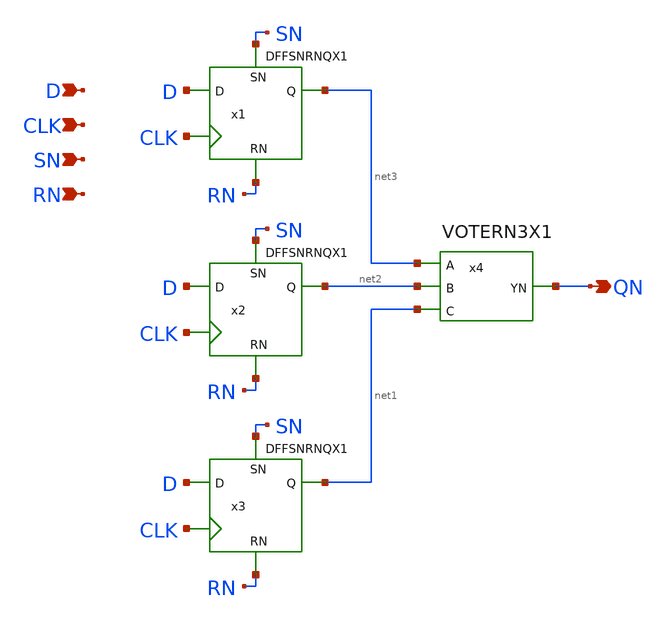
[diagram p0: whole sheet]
** sch_path: lib/xschem/TMRDFFSNRNQNX1.sch
**.subckt TMRDFFSNRNQNX1 QN D CLK SN RN
*.opin QN
*.ipin D
*.ipin CLK
*.ipin SN
*.ipin RN
x4 net3 net2 net1 QN VDD VSS VOTERN3X1
x1 net3 D CLK SN RN VDD VSS DFFSNRNQX1
x2 net2 D CLK SN RN VDD VSS DFFSNRNQX1
x3 net1 D CLK SN RN VDD VSS DFFSNRNQX1
**.ends

* expanding   symbol:  VOTERN3X1.sym # of pins=4
** sym_path: VOTERN3X1.sym
** sch_path: VOTERN3X1.sch
.subckt VOTERN3X1 A B C YN VDD VSS
*.opin YN
*.ipin A
*.ipin B
*.ipin C
XM2 net1 A VDD VDD sky130_fd_pr__pfet_01v8 L=0.15 W=2 nf=1 ad='int((nf+1)/2) * W/nf * 0.29' as='int((nf+2)/2) * W/nf * 0.29'
+ pd='2*int((nf+1)/2) * (W/nf + 0.29)' ps='2*int((nf+2)/2) * (W/nf + 0.29)' nrd='0.29 / W' nrs='0.29 / W'
+ sa=0 sb=0 sd=0 mult=2 m=2
XM3 net2 B VSS VSS sky130_fd_pr__nfet_01v8 L=0.15 W=3 nf=1 ad='int((nf+1)/2) * W/nf * 0.29' as='int((nf+2)/2) * W/nf * 0.29'
+ pd='2*int((nf+1)/2) * (W/nf + 0.29)' ps='2*int((nf+2)/2) * (W/nf + 0.29)' nrd='0.29 / W' nrs='0.29 / W'
+ sa=0 sb=0 sd=0 mult=1 m=1
XM4 YN A net2 VSS sky130_fd_pr__nfet_01v8 L=0.15 W=3 nf=1 ad='int((nf+1)/2) * W/nf * 0.29' as='int((nf+2)/2) * W/nf * 0.29'
+ pd='2*int((nf+1)/2) * (W/nf + 0.29)' ps='2*int((nf+2)/2) * (W/nf + 0.29)' nrd='0.29 / W' nrs='0.29 / W'
+ sa=0 sb=0 sd=0 mult=1 m=1
XM1 net1 B VDD VDD sky130_fd_pr__pfet_01v8 L=0.15 W=2 nf=1 ad='int((nf+1)/2) * W/nf * 0.29' as='int((nf+2)/2) * W/nf * 0.29'
+ pd='2*int((nf+1)/2) * (W/nf + 0.29)' ps='2*int((nf+2)/2) * (W/nf + 0.29)' nrd='0.29 / W' nrs='0.29 / W'
+ sa=0 sb=0 sd=0 mult=2 m=2
XM5 net3 B net1 VDD sky130_fd_pr__pfet_01v8 L=0.15 W=2 nf=1 ad='int((nf+1)/2) * W/nf * 0.29' as='int((nf+2)/2) * W/nf * 0.29'
+ pd='2*int((nf+1)/2) * (W/nf + 0.29)' ps='2*int((nf+2)/2) * (W/nf + 0.29)' nrd='0.29 / W' nrs='0.29 / W'
+ sa=0 sb=0 sd=0 mult=2 m=2
XM6 YN C net3 VDD sky130_fd_pr__pfet_01v8 L=0.15 W=2 nf=1 ad='int((nf+1)/2) * W/nf * 0.29' as='int((nf+2)/2) * W/nf * 0.29'
+ pd='2*int((nf+1)/2) * (W/nf + 0.29)' ps='2*int((nf+2)/2) * (W/nf + 0.29)' nrd='0.29 / W' nrs='0.29 / W'
+ sa=0 sb=0 sd=0 mult=2 m=2
XM7 net3 C net1 VDD sky130_fd_pr__pfet_01v8 L=0.15 W=2 nf=1 ad='int((nf+1)/2) * W/nf * 0.29' as='int((nf+2)/2) * W/nf * 0.29'
+ pd='2*int((nf+1)/2) * (W/nf + 0.29)' ps='2*int((nf+2)/2) * (W/nf + 0.29)' nrd='0.29 / W' nrs='0.29 / W'
+ sa=0 sb=0 sd=0 mult=2 m=2
XM10 YN A net3 VDD sky130_fd_pr__pfet_01v8 L=0.15 W=2 nf=1 ad='int((nf+1)/2) * W/nf * 0.29' as='int((nf+2)/2) * W/nf * 0.29'
+ pd='2*int((nf+1)/2) * (W/nf + 0.29)' ps='2*int((nf+2)/2) * (W/nf + 0.29)' nrd='0.29 / W' nrs='0.29 / W'
+ sa=0 sb=0 sd=0 mult=2 m=2
XM8 net4 B VSS VSS sky130_fd_pr__nfet_01v8 L=0.15 W=3 nf=1 ad='int((nf+1)/2) * W/nf * 0.29' as='int((nf+2)/2) * W/nf * 0.29'
+ pd='2*int((nf+1)/2) * (W/nf + 0.29)' ps='2*int((nf+2)/2) * (W/nf + 0.29)' nrd='0.29 / W' nrs='0.29 / W'
+ sa=0 sb=0 sd=0 mult=1 m=1
XM9 YN C net4 VSS sky130_fd_pr__nfet_01v8 L=0.15 W=3 nf=1 ad='int((nf+1)/2) * W/nf * 0.29' as='int((nf+2)/2) * W/nf * 0.29'
+ pd='2*int((nf+1)/2) * (W/nf + 0.29)' ps='2*int((nf+2)/2) * (W/nf + 0.29)' nrd='0.29 / W' nrs='0.29 / W'
+ sa=0 sb=0 sd=0 mult=1 m=1
XM11 net5 C VSS VSS sky130_fd_pr__nfet_01v8 L=0.15 W=3 nf=1 ad='int((nf+1)/2) * W/nf * 0.29' as='int((nf+2)/2) * W/nf * 0.29'
+ pd='2*int((nf+1)/2) * (W/nf + 0.29)' ps='2*int((nf+2)/2) * (W/nf + 0.29)' nrd='0.29 / W' nrs='0.29 / W'
+ sa=0 sb=0 sd=0 mult=1 m=1
XM12 YN A net5 VSS sky130_fd_pr__nfet_01v8 L=0.15 W=3 nf=1 ad='int((nf+1)/2) * W/nf * 0.29' as='int((nf+2)/2) * W/nf * 0.29'
+ pd='2*int((nf+1)/2) * (W/nf + 0.29)' ps='2*int((nf+2)/2) * (W/nf + 0.29)' nrd='0.29 / W' nrs='0.29 / W'
+ sa=0 sb=0 sd=0 mult=1 m=1
.ends

.end
